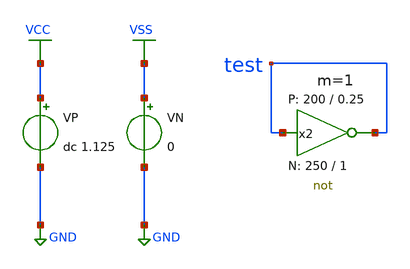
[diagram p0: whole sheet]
** sch_path: Amplifier_Inv/xschem/inv_tb.sch
* StefanSchippers/xschem_sky130/sky130_tests/not.sch:
* Copyright 2021 Stefan Frederik Schippers
* Licensed under the Apache License, Version 2.0 (the "License");
**.subckt inv_tb
x2 test test VCC VSS not W_N=250 L_N=1 W_P=200 L_P=0.25 m=1
VN VSS GND 0
VP VCC GND dc 1.125
**** begin user architecture code

** opencircuitdesign pdks install
.lib $::SKYWATER_MODELS/sky130.lib.spice tt



.control

  tran 0.1u 50m
  save all
  write inv_tb.raw
  exit 0
.endc


**** end user architecture code
**.ends

* expanding   symbol:  sky130_tests/not.sym # of pins=2
** sym_path: sky130_tests/not.sym
** sch_path: sky130_tests/not.sch
.subckt not y a VCCPIN VSSPIN     W_N=1 L_N=0.15 W_P=2 L_P=0.15
*.opin y
*.ipin a
XM1 DN a VSSPIN VSSPIN sky130_fd_pr__nfet_01v8 L=L_N W=W_N nf=1 ad='int((1 + 1)/2) * W_N / 1 * 0.29'
+ as='int((1 + 2)/2) * W_N / 1 * 0.29' pd='2*int((1 + 1)/2) * (W_N / 1 + 0.29)' ps='2*int((1 + 2)/2) * (W_N / 1 + 0.29)'
+ nrd='0.29 / W_N ' nrs='0.29 / W_N ' sa=0 sb=0 sd=0 mult=1 m=1
XM2 DP a VCCPIN VCCPIN sky130_fd_pr__pfet_01v8 L=L_P W=W_P nf=1 ad='int((nf+1)/2) * W/nf * 0.29' as='int((nf+2)/2) * W/nf * 0.29'
+ pd='2*int((nf+1)/2) * (W/nf + 0.29)' ps='2*int((nf+2)/2) * (W/nf + 0.29)' nrd='0.29 / W' nrs='0.29 / W'
+ sa=0 sb=0 sd=0 mult=1 m=1
Vmeas DP y 0
.save i(vmeas)
Vmeas1 y DN 0
.save i(vmeas1)
.save v(dp)
.save v(dn)
.ends

.GLOBAL GND
.GLOBAL VSS
.GLOBAL VCC
.end
